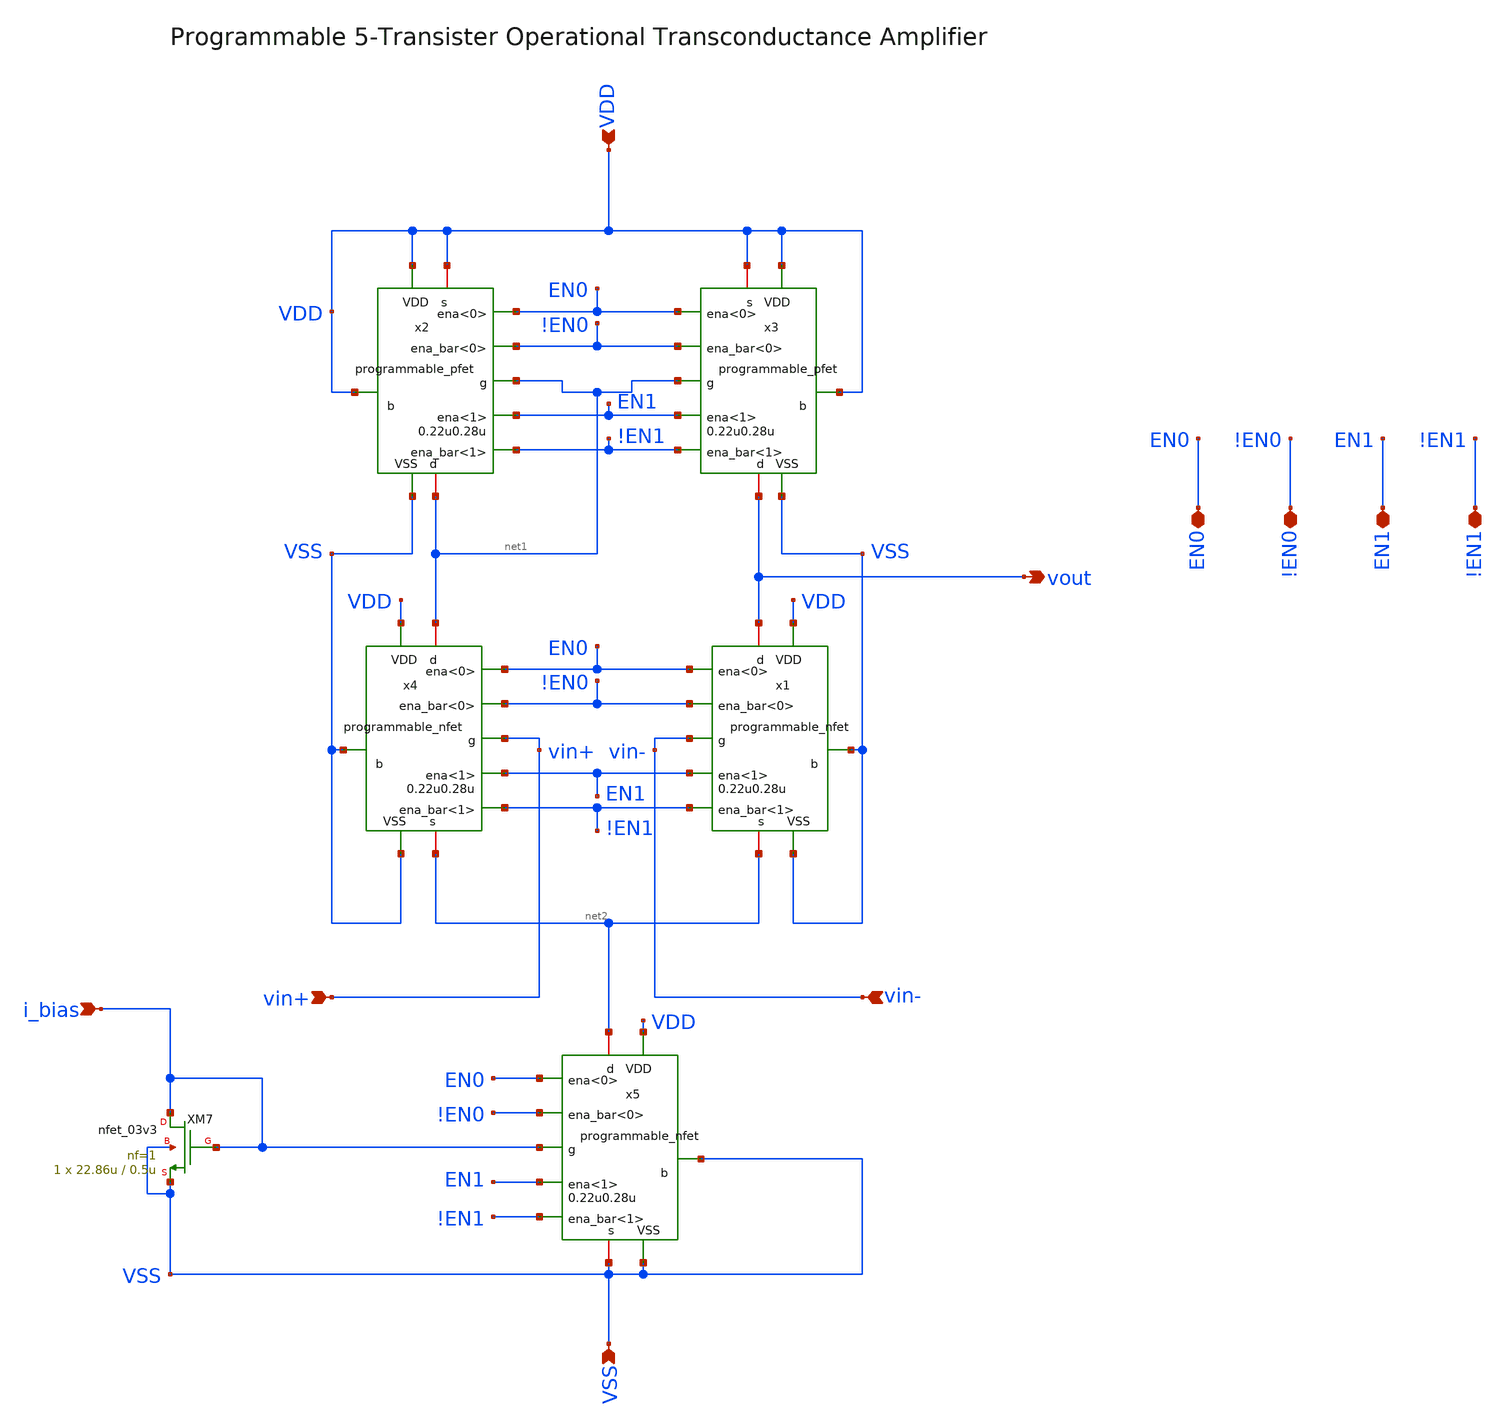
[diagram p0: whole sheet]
** sch_path: designs/libs/core_amps/ota_5t/5tOTA_programble.sch
**.subckt 5tOTA_programble i_bias vout vin+ vin- EN0 !EN0 EN1 !EN1 VDD VSS
*.ipin i_bias
*.opin vout
*.ipin vin+
*.ipin vin-
*.iopin EN0
*.iopin !EN0
*.iopin EN1
*.iopin !EN1
*.ipin VDD
*.ipin VSS
x1 vout VSS vin- net2 !EN0 VDD !EN1 EN0 EN1 VSS programmable_nfet width=0.22u length=0.28u
x2 net1 VDD net1 VDD !EN0 VDD !EN1 EN0 EN1 VSS programmable_pfet width=0.22u length=0.28u
x3 vout VDD net1 VDD !EN0 VDD !EN1 EN0 EN1 VSS programmable_pfet width=0.22u length=0.28u
x4 net1 VSS vin+ net2 !EN0 VDD !EN1 EN0 EN1 VSS programmable_nfet width=0.22u length=0.28u
x5 net2 VSS i_bias VSS !EN0 VDD !EN1 EN0 EN1 VSS programmable_nfet width=0.22u length=0.28u
XM7 i_bias i_bias VSS VSS nfet_03v3 L=0.5u W=22.86u nf=1 ad='int((nf+1)/2) * W/nf * 0.18u' as='int((nf+2)/2) * W/nf * 0.18u'
+ pd='2*int((nf+1)/2) * (W/nf + 0.18u)' ps='2*int((nf+2)/2) * (W/nf + 0.18u)' nrd='0.18u / W' nrs='0.18u / W'
+ sa=0 sb=0 sd=0 m=1
**.ends
.end
